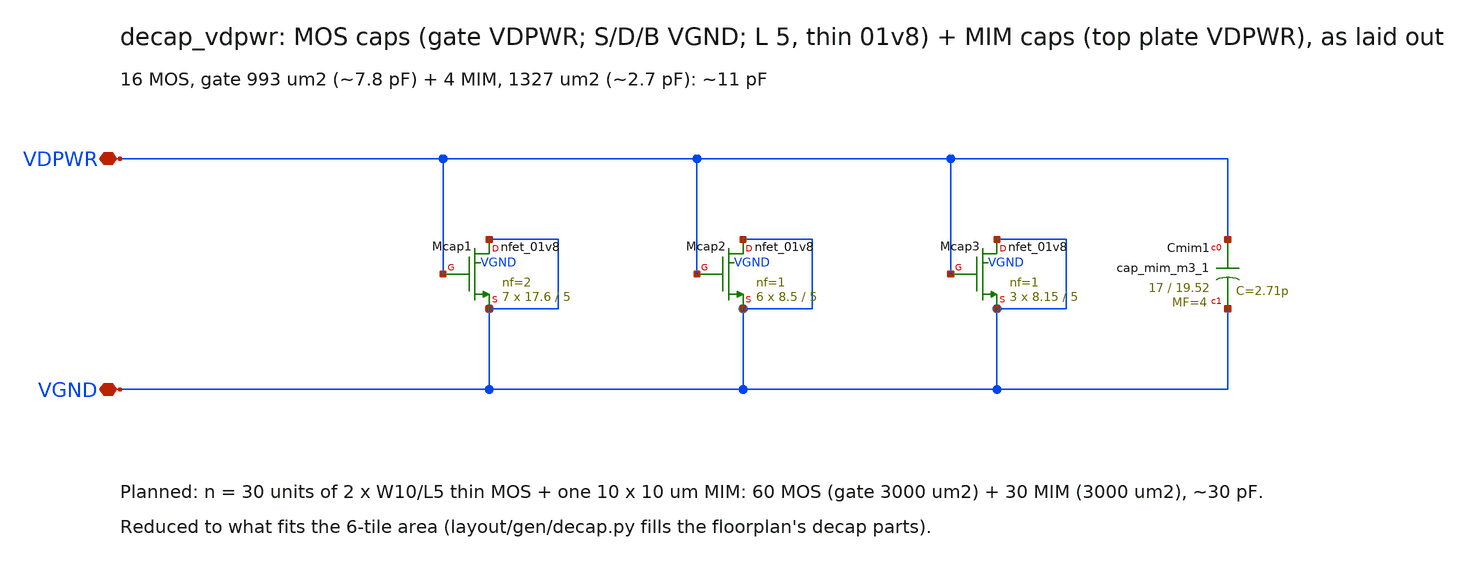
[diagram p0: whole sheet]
** sch_path: xschem/decap_vdpwr.sch
**.subckt decap_vdpwr VDPWR VGND
*.iopin VDPWR
*.iopin VGND
XMcap1 VGND VDPWR VGND VGND sky130_fd_pr__nfet_01v8 L=5 W=17.6 nf=2 ad='int((nf+1)/2) * W/nf * 0.29'
+ as='int((nf+2)/2) * W/nf * 0.29' pd='2*int((nf+1)/2) * (W/nf + 0.29)' ps='2*int((nf+2)/2) * (W/nf + 0.29)'
+ nrd='0.29 / W' nrs='0.29 / W' sa=0 sb=0 sd=0 mult=7 m=7
XMcap2 VGND VDPWR VGND VGND sky130_fd_pr__nfet_01v8 L=5 W=8.5 nf=1 ad='int((nf+1)/2) * W/nf * 0.29' as='int((nf+2)/2) * W/nf * 0.29'
+ pd='2*int((nf+1)/2) * (W/nf + 0.29)' ps='2*int((nf+2)/2) * (W/nf + 0.29)' nrd='0.29 / W' nrs='0.29 / W'
+ sa=0 sb=0 sd=0 mult=6 m=6
XMcap3 VGND VDPWR VGND VGND sky130_fd_pr__nfet_01v8 L=5 W=8.15 nf=1 ad='int((nf+1)/2) * W/nf * 0.29'
+ as='int((nf+2)/2) * W/nf * 0.29' pd='2*int((nf+1)/2) * (W/nf + 0.29)' ps='2*int((nf+2)/2) * (W/nf + 0.29)'
+ nrd='0.29 / W' nrs='0.29 / W' sa=0 sb=0 sd=0 mult=3 m=3
XCmim1 VDPWR VGND sky130_fd_pr__cap_mim_m3_1 W=17 L=19.52 MF=4 m=4
**.ends
.end
